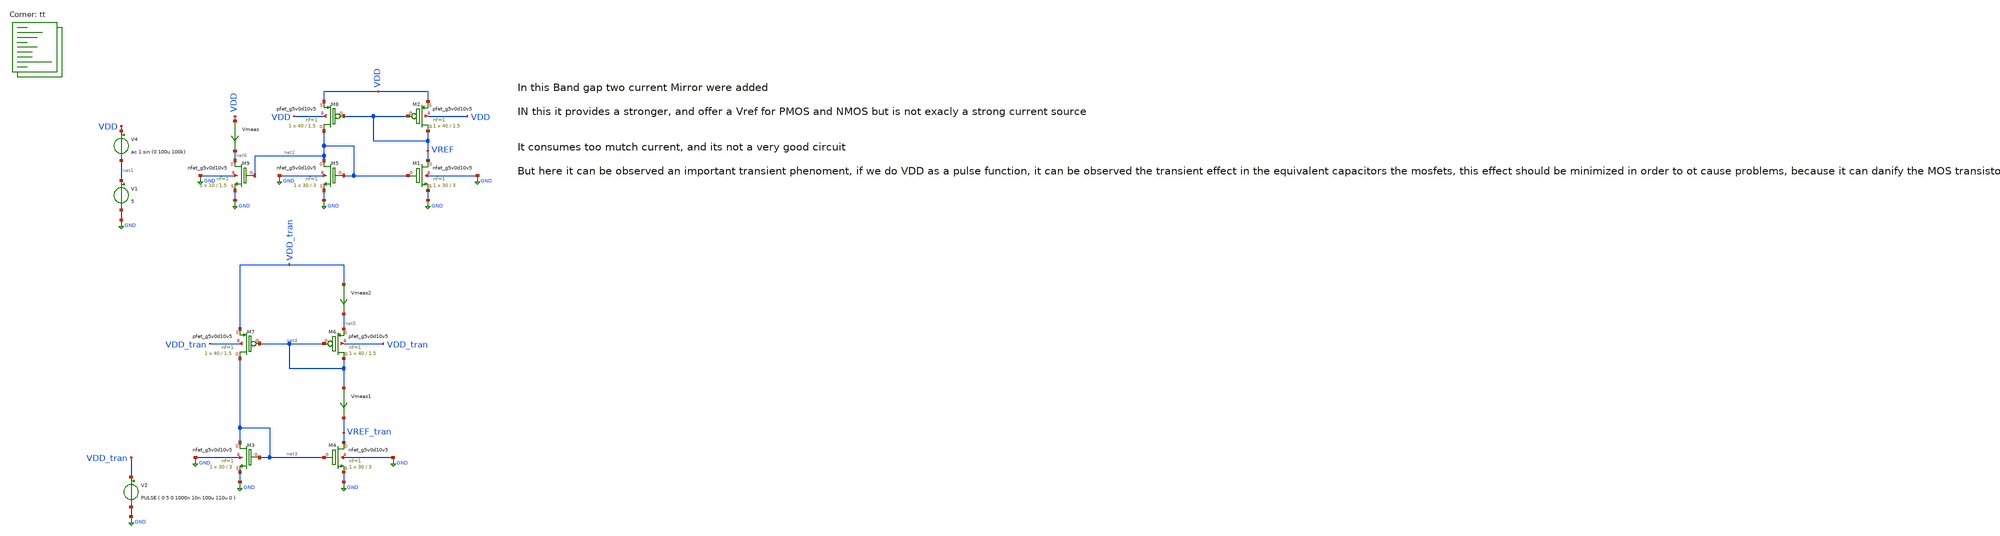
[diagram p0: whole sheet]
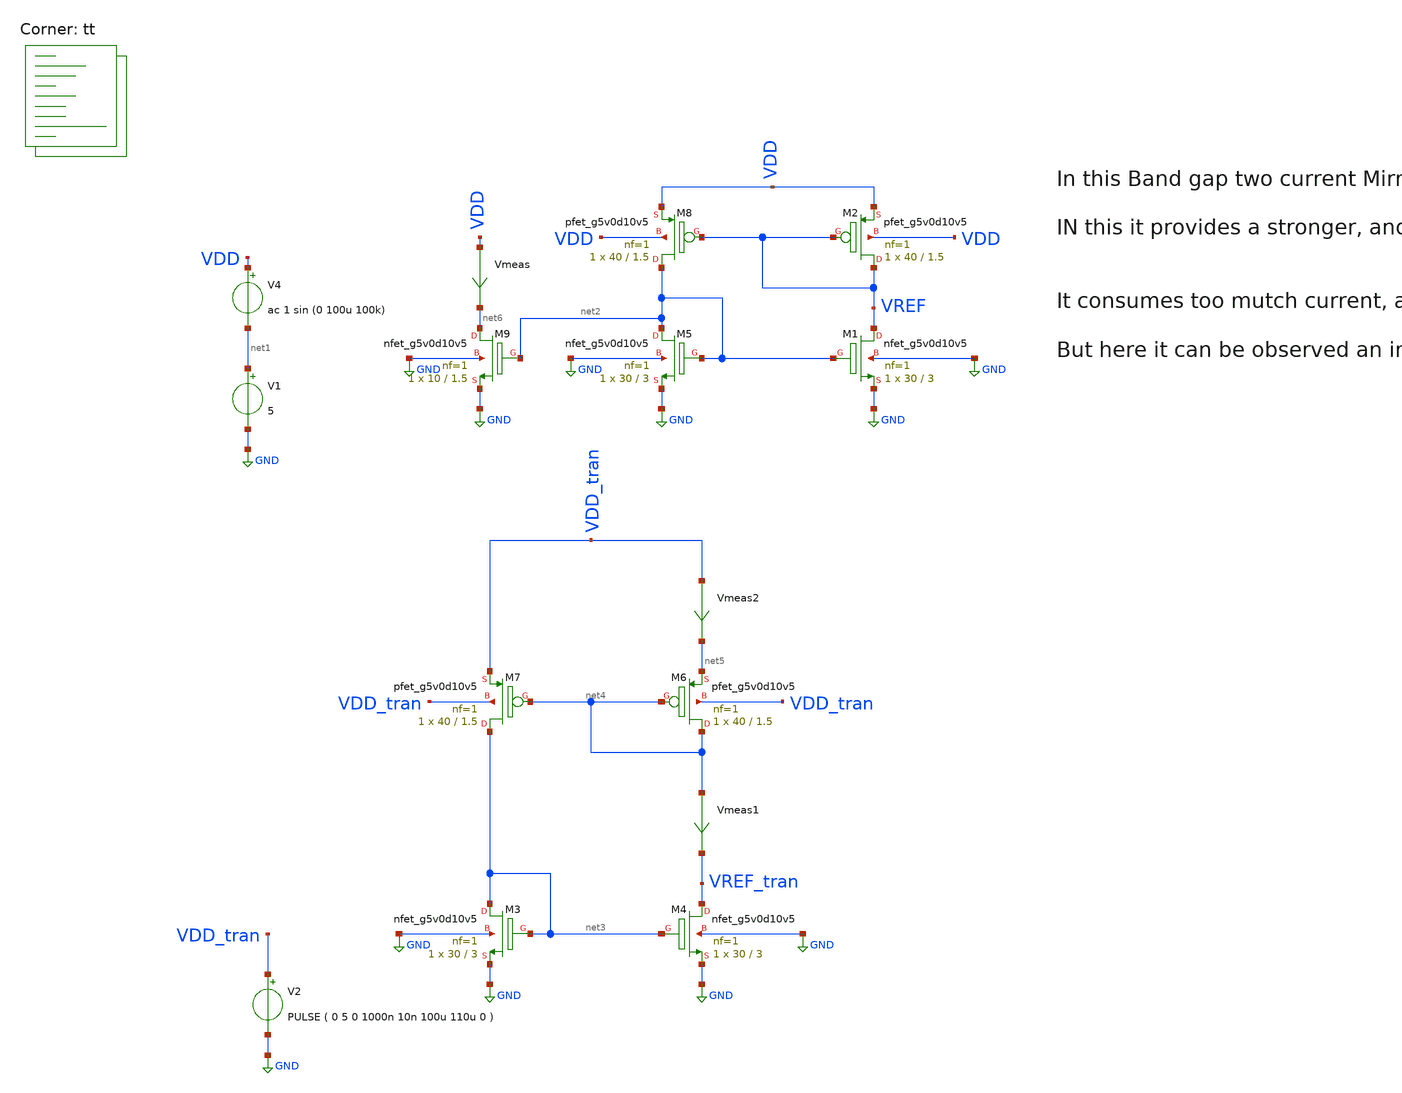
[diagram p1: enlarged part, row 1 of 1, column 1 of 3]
** sch_path: bandgaps/nmos_bandgap/bandgap.sch
**.subckt bandgap
V1 net1 GND 5
V2 VDD_tran GND PULSE ( 0 5 0 1000n 10n 100u 110u 0 )
XM6 net4 net4 net5 VDD_tran sky130_fd_pr__pfet_g5v0d10v5 L=1.5 W=40 nf=1 ad='int((1 + 1)/2) * 40 / 1 * 0.29'
+ as='int((1 + 2)/2) * 40 / 1 * 0.29' pd='2*int((1 + 1)/2) * (40 / 1 + 0.29)' ps='2*int((1 + 2)/2) * (40 / 1 + 0.29)'
+ nrd='0.29 / 40 ' nrs='0.29 / 40 ' sa=0 sb=0 sd=0 mult=1 m=1
XM7 net3 net4 VDD_tran VDD_tran sky130_fd_pr__pfet_g5v0d10v5 L=1.5 W=40 nf=1 ad='int((1 + 1)/2) * 40 / 1 * 0.29'
+ as='int((1 + 2)/2) * 40 / 1 * 0.29' pd='2*int((1 + 1)/2) * (40 / 1 + 0.29)' ps='2*int((1 + 2)/2) * (40 / 1 + 0.29)'
+ nrd='0.29 / 40 ' nrs='0.29 / 40 ' sa=0 sb=0 sd=0 mult=1 m=1
XM3 net3 net3 GND GND sky130_fd_pr__nfet_g5v0d10v5 L=3 W=30 nf=1 ad='int((1 + 1)/2) * 30 / 1 * 0.29'
+ as='int((1 + 2)/2) * 30 / 1 * 0.29' pd='2*int((1 + 1)/2) * (30 / 1 + 0.29)' ps='2*int((1 + 2)/2) * (30 / 1 + 0.29)'
+ nrd='0.29 / 30 ' nrs='0.29 / 30 ' sa=0 sb=0 sd=0 mult=1 m=1
XM4 VREF_tran net3 GND GND sky130_fd_pr__nfet_g5v0d10v5 L=3 W=30 nf=1 ad='int((1 + 1)/2) * 30 / 1 * 0.29'
+ as='int((1 + 2)/2) * 30 / 1 * 0.29' pd='2*int((1 + 1)/2) * (30 / 1 + 0.29)' ps='2*int((1 + 2)/2) * (30 / 1 + 0.29)'
+ nrd='0.29 / 30 ' nrs='0.29 / 30 ' sa=0 sb=0 sd=0 mult=1 m=1
XM5 net2 net2 GND GND sky130_fd_pr__nfet_g5v0d10v5 L=3 W=30 nf=1 ad='int((1 + 1)/2) * 30 / 1 * 0.29'
+ as='int((1 + 2)/2) * 30 / 1 * 0.29' pd='2*int((1 + 1)/2) * (30 / 1 + 0.29)' ps='2*int((1 + 2)/2) * (30 / 1 + 0.29)'
+ nrd='0.29 / 30 ' nrs='0.29 / 30 ' sa=0 sb=0 sd=0 mult=1 m=1
XM1 VREF net2 GND GND sky130_fd_pr__nfet_g5v0d10v5 L=3 W=30 nf=1 ad='int((1 + 1)/2) * 30 / 1 * 0.29'
+ as='int((1 + 2)/2) * 30 / 1 * 0.29' pd='2*int((1 + 1)/2) * (30 / 1 + 0.29)' ps='2*int((1 + 2)/2) * (30 / 1 + 0.29)'
+ nrd='0.29 / 30 ' nrs='0.29 / 30 ' sa=0 sb=0 sd=0 mult=1 m=1
XM2 VREF VREF VDD VDD sky130_fd_pr__pfet_g5v0d10v5 L=1.5 W=40 nf=1 ad='int((1 + 1)/2) * 40 / 1 * 0.29'
+ as='int((1 + 2)/2) * 40 / 1 * 0.29' pd='2*int((1 + 1)/2) * (40 / 1 + 0.29)' ps='2*int((1 + 2)/2) * (40 / 1 + 0.29)'
+ nrd='0.29 / 40 ' nrs='0.29 / 40 ' sa=0 sb=0 sd=0 mult=1 m=1
XM8 net2 VREF VDD VDD sky130_fd_pr__pfet_g5v0d10v5 L=1.5 W=40 nf=1 ad='int((1 + 1)/2) * 40 / 1 * 0.29'
+ as='int((1 + 2)/2) * 40 / 1 * 0.29' pd='2*int((1 + 1)/2) * (40 / 1 + 0.29)' ps='2*int((1 + 2)/2) * (40 / 1 + 0.29)'
+ nrd='0.29 / 40 ' nrs='0.29 / 40 ' sa=0 sb=0 sd=0 mult=1 m=1
V4 VDD net1 ac 1 sin (0 100u 100k)
XM9 net6 net2 GND GND sky130_fd_pr__nfet_g5v0d10v5 L=1.5 W=10 nf=1 ad='int((1 + 1)/2) * 10 / 1 * 0.29'
+ as='int((1 + 2)/2) * 10 / 1 * 0.29' pd='2*int((1 + 1)/2) * (10 / 1 + 0.29)' ps='2*int((1 + 2)/2) * (10 / 1 + 0.29)'
+ nrd='0.29 / 10 ' nrs='0.29 / 10 ' sa=0 sb=0 sd=0 mult=1 m=1
Vmeas VDD net6 0
.save i(vmeas)
Vmeas1 net4 VREF_tran 0
.save i(vmeas1)
Vmeas2 VDD_tran net5 0
.save i(vmeas2)
**** begin user architecture code

**************************************************************
**************************************************************
**************************************************************
**************************************************************
**************************************************************
*LIBs*********************************************************
**************************************************************
**************************************************************
**************************************************************
**************************************************************
**************************************************************
*.lib $::SKYWATER_MODELS/sky130.lib.spice tt
* chose the corners in the corner file
* tt_mm for mismatch
* ss ff sf fs standart corners
* ll hh lh hl capacitor and resistors corners
* mc for total process variation including corners
**************************************************************
**************************************************************
**************************************************************
**************************************************************
**************************************************************
*Corners/montecarlo options***********************************
**************************************************************
**************************************************************
**************************************************************
**************************************************************
**************************************************************
.TEMP 27
**************************************************************
**************************************************************
**************************************************************
**************************************************************
*SIMULATION and Plots*****************************************
**************************************************************
**************************************************************
**************************************************************
**************************************************************
.control
save all
dc TEMP -20 140 0.01
plot v(VREF)
plot i(VMEAS)
tran 10ns 10us
plot v(VREF_tran)
plot i(VMEAS1)  i(VMEAS2)
ac dec 20 1 1000G
plot db(v(VREF))

.endc

.lib $::SKYWATER_MODELS/sky130.lib.spice tt
**** end user architecture code
**.ends
.GLOBAL GND
.end
